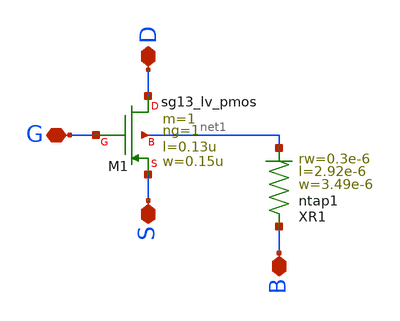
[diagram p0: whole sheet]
** sch_path: ihp-sg13cmos5l/schematic/xschem/sg13_lv_pmos_ring_pcell.sch
**.subckt sg13_lv_pmos_ring_pcell D S G B
*.iopin D
*.iopin S
*.iopin G
*.iopin B
XM1 D G S net1 sg13_lv_pmos w=0.15u l=0.13u ng=1 m=1 mm_ok=1
XR1 B net1 ntap1 R=19.61 w=3.49e-6 l=2.92e-6 rw=0.3e-6
**.ends
.end
